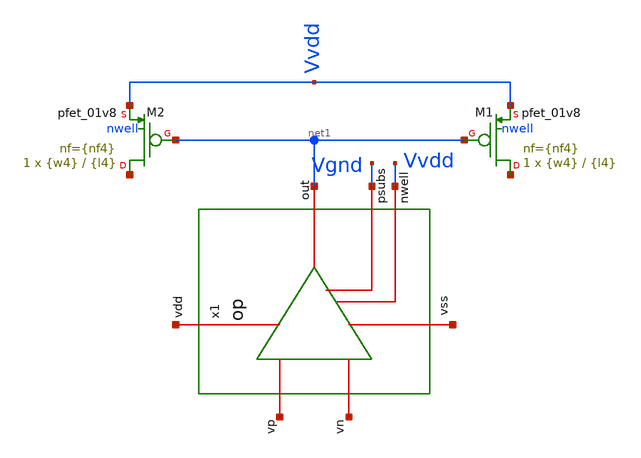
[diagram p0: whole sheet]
** sch_path: xschem/bgr_op.sch
**.subckt bgr_op
x1 net1 net2 net3 net4 net5 Vgnd Vvdd op
XM1 net6 net1 Vvdd nwell sky130_fd_pr__pfet_01v8 L={l4} W={w4} nf={nf4} ad='int(({nf4} + 1)/2) * {w4} / {nf4} * 0.29'
+ as='int(({nf4} + 2)/2) * {w4} / {nf4} * 0.29' pd='2*int(({nf4} + 1)/2) * ({w4} / {nf4} + 0.29)' ps='2*int(({nf4} + 2)/2) * ({w4} / {nf4} + 0.29)'
+ nrd='0.29 / {w4} ' nrs='0.29 / {w4} ' sa=0 sb=0 sd=0 mult=1 m=1
XM2 net7 net1 Vvdd nwell sky130_fd_pr__pfet_01v8 L={l4} W={w4} nf={nf4} ad='int(({nf4} + 1)/2) * {w4} / {nf4} * 0.29'
+ as='int(({nf4} + 2)/2) * {w4} / {nf4} * 0.29' pd='2*int(({nf4} + 1)/2) * ({w4} / {nf4} + 0.29)' ps='2*int(({nf4} + 2)/2) * ({w4} / {nf4} + 0.29)'
+ nrd='0.29 / {w4} ' nrs='0.29 / {w4} ' sa=0 sb=0 sd=0 mult=1 m=1
**.ends

* expanding   symbol:  op.sym # of pins=7
** sym_path: xschem/op.sym
** sch_path: xschem/op.sch
.subckt op out vdd vss vp vn psubs nwell
*.iopin vss
*.iopin vdd
*.opin out
*.ipin vp
*.ipin vn
*.iopin psubs
*.iopin nwell
XM3 out net1 vdd nwell sky130_fd_pr__pfet_01v8 L={l3} W={w3} nf={nf3} ad='int((nf+1)/2) * W/nf * 0.29'
+ as='int((nf+2)/2) * W/nf * 0.29' pd='2*int((nf+1)/2) * (W/nf + 0.29)' ps='2*int((nf+2)/2) * (W/nf + 0.29)'
+ nrd='0.29 / W' nrs='0.29 / W' sa=0 sb=0 sd=0 mult=1 m=1
XM1b net1 vn net2 psubs sky130_fd_pr__nfet_01v8 L={l1} W={w1} nf={nf1} ad='int((nf+1)/2) * W/nf * 0.29'
+ as='int((nf+2)/2) * W/nf * 0.29' pd='2*int((nf+1)/2) * (W/nf + 0.29)' ps='2*int((nf+2)/2) * (W/nf + 0.29)'
+ nrd='0.29 / W' nrs='0.29 / W' sa=0 sb=0 sd=0 mult=1 m=1
XM1a net3 vp net2 psubs sky130_fd_pr__nfet_01v8 L={l1} W={w1} nf={nf1} ad='int((nf+1)/2) * W/nf * 0.29'
+ as='int((nf+2)/2) * W/nf * 0.29' pd='2*int((nf+1)/2) * (W/nf + 0.29)' ps='2*int((nf+2)/2) * (W/nf + 0.29)'
+ nrd='0.29 / W' nrs='0.29 / W' sa=0 sb=0 sd=0 mult=1 m=1
XR1 net4 net1 vss sky130_fd_pr__res_high_po_0p35 L={lrz} mult=1 m=1
XC1 out net4 sky130_fd_pr__cap_mim_m3_1 W={wc} L={wc} MF={mc} m={mc}
**** begin user architecture code


.include ../sizing_opamp.spice


**** end user architecture code
XM2a net3 net3 vdd nwell sky130_fd_pr__pfet_01v8 L={l2} W={w2} nf={nf2} ad='int(({nf2} + 1)/2) * {w2} / {nf2} * 0.29'
+ as='int(({nf2} + 2)/2) * {w2} / {nf2} * 0.29' pd='2*int(({nf2} + 1)/2) * ({w2} / {nf2} + 0.29)' ps='2*int(({nf2} + 2)/2) * ({w2} / {nf2} + 0.29)'
+ nrd='0.29 / {w2} ' nrs='0.29 / {w2} ' sa=0 sb=0 sd=0 mult=1 m=1
XM2b net1 net3 vdd nwell sky130_fd_pr__pfet_01v8 L={l2} W={w2} nf={nf2} ad='int(({nf2} + 1)/2) * {w2} / {nf2} * 0.29'
+ as='int(({nf2} + 2)/2) * {w2} / {nf2} * 0.29' pd='2*int(({nf2} + 1)/2) * ({w2} / {nf2} + 0.29)' ps='2*int(({nf2} + 2)/2) * ({w2} / {nf2} + 0.29)'
+ nrd='0.29 / {w2} ' nrs='0.29 / {w2} ' sa=0 sb=0 sd=0 mult=1 m=1
XM0a bias bias vss psubs sky130_fd_pr__nfet_01v8 L={l0} W={w0} nf={nf0} ad='int(({nf0} + 1)/2) * {w0} / {nf0} * 0.29'
+ as='int(({nf0} + 2)/2) * {w0} / {nf0} * 0.29' pd='2*int(({nf0} + 1)/2) * ({w0} / {nf0} + 0.29)' ps='2*int(({nf0} + 2)/2) * ({w0} / {nf0} + 0.29)'
+ nrd='0.29 / {w0} ' nrs='0.29 / {w0} ' sa=0 sb=0 sd=0 mult=1 m=1
I0 vdd bias {i_tail}
XM0b net2 bias vss psubs sky130_fd_pr__nfet_01v8 L={l0} W={w0} nf={nf0} ad='int(({nf0} + 1)/2) * {w0} / {nf0} * 0.29'
+ as='int(({nf0} + 2)/2) * {w0} / {nf0} * 0.29' pd='2*int(({nf0} + 1)/2) * ({w0} / {nf0} + 0.29)' ps='2*int(({nf0} + 2)/2) * ({w0} / {nf0} + 0.29)'
+ nrd='0.29 / {w0} ' nrs='0.29 / {w0} ' sa=0 sb=0 sd=0 mult=1 m=1
XM0c out bias vss psubs sky130_fd_pr__nfet_01v8 L={l0} W={w0} nf={nf0} ad='int(({nf0} + 1)/2) * {w0} / {nf0} * 0.29'
+ as='int(({nf0} + 2)/2) * {w0} / {nf0} * 0.29' pd='2*int(({nf0} + 1)/2) * ({w0} / {nf0} + 0.29)' ps='2*int(({nf0} + 2)/2) * ({w0} / {nf0} + 0.29)'
+ nrd='0.29 / {w0} ' nrs='0.29 / {w0} ' sa=0 sb=0 sd=0 mult=1 m=1
.ends

.end
